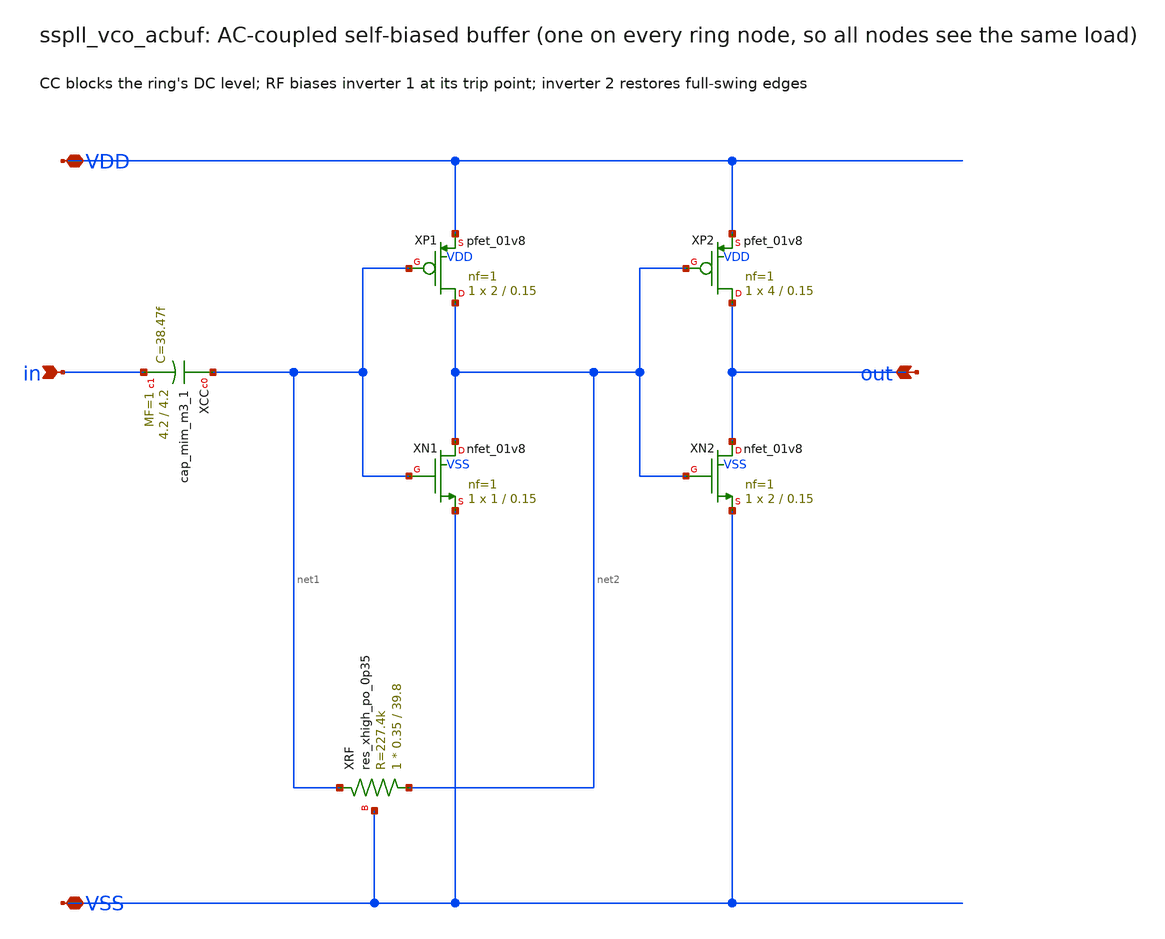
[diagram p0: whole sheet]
** sch_path: xschem/vco/sspll_vco_acbuf.sch
**.subckt sspll_vco_acbuf VDD VSS in out
*.iopin VDD
*.iopin VSS
*.ipin in
*.opin out
XXCC net1 in sky130_fd_pr__cap_mim_m3_1 W=4.2 L=4.2 MF=1 m=1
XXP1 net2 net1 VDD VDD sky130_fd_pr__pfet_01v8 L=0.15 W=2 nf=1 ad='int((nf+1)/2) * W/nf * 0.29' as='int((nf+2)/2) * W/nf * 0.29'
+ pd='2*int((nf+1)/2) * (W/nf + 0.29)' ps='2*int((nf+2)/2) * (W/nf + 0.29)' nrd='0.29 / W' nrs='0.29 / W'
+ sa=0 sb=0 sd=0 mult=1 m=1
XXN1 net2 net1 VSS VSS sky130_fd_pr__nfet_01v8 L=0.15 W=1 nf=1 ad='int((nf+1)/2) * W/nf * 0.29' as='int((nf+2)/2) * W/nf * 0.29'
+ pd='2*int((nf+1)/2) * (W/nf + 0.29)' ps='2*int((nf+2)/2) * (W/nf + 0.29)' nrd='0.29 / W' nrs='0.29 / W'
+ sa=0 sb=0 sd=0 mult=1 m=1
XXRF net2 net1 VSS sky130_fd_pr__res_xhigh_po_0p35 L=39.8 mult=1 m=1
XXP2 out net2 VDD VDD sky130_fd_pr__pfet_01v8 L=0.15 W=4 nf=1 ad='int((nf+1)/2) * W/nf * 0.29' as='int((nf+2)/2) * W/nf * 0.29'
+ pd='2*int((nf+1)/2) * (W/nf + 0.29)' ps='2*int((nf+2)/2) * (W/nf + 0.29)' nrd='0.29 / W' nrs='0.29 / W'
+ sa=0 sb=0 sd=0 mult=1 m=1
XXN2 out net2 VSS VSS sky130_fd_pr__nfet_01v8 L=0.15 W=2 nf=1 ad='int((nf+1)/2) * W/nf * 0.29' as='int((nf+2)/2) * W/nf * 0.29'
+ pd='2*int((nf+1)/2) * (W/nf + 0.29)' ps='2*int((nf+2)/2) * (W/nf + 0.29)' nrd='0.29 / W' nrs='0.29 / W'
+ sa=0 sb=0 sd=0 mult=1 m=1
**.ends
.end
